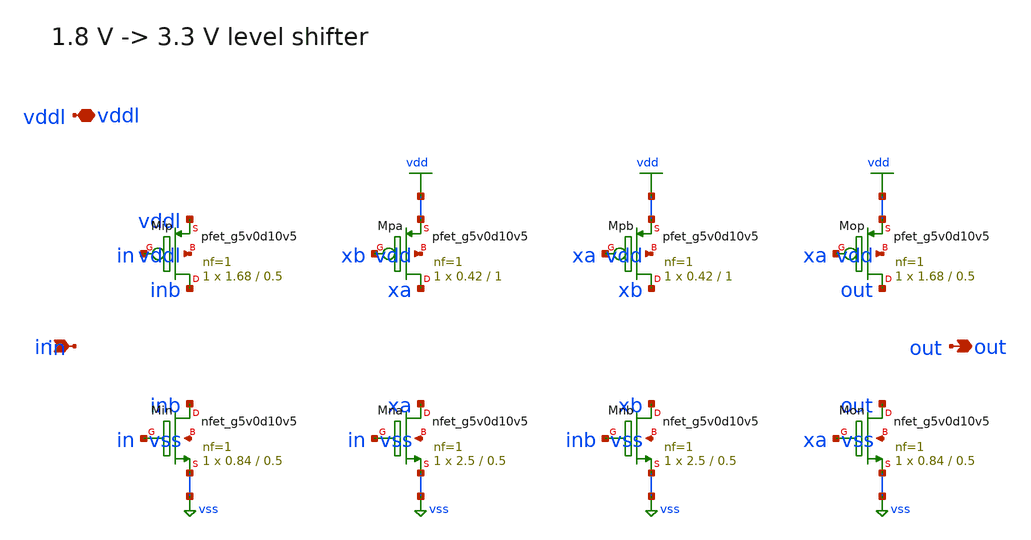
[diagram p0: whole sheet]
** sch_path: xschem/rt5w_lsup.sch
**.subckt rt5w_lsup in out vddl
*.ipin in
*.opin out
*.iopin vddl
XMip inb in vddl vddl sky130_fd_pr__pfet_g5v0d10v5 L=0.5 W=1.68 nf=1 ad=0.4872 as=0.4872 pd=3.94
+ ps=3.94 nrd=0.1726 nrs=0.1726 sa=0 sb=0 sd=0 mult=1 m=1
XMin inb in vss vss sky130_fd_pr__nfet_g5v0d10v5 L=0.5 W=0.84 nf=1 ad=0.2436 as=0.2436 pd=2.26
+ ps=2.26 nrd=0.3452 nrs=0.3452 sa=0 sb=0 sd=0 mult=1 m=1
XMpa xa xb vdd vdd sky130_fd_pr__pfet_g5v0d10v5 L=1 W=0.42 nf=1 ad=0.1218 as=0.1218 pd=1.42 ps=1.42
+ nrd=0.6905 nrs=0.6905 sa=0 sb=0 sd=0 mult=1 m=1
XMpb xb xa vdd vdd sky130_fd_pr__pfet_g5v0d10v5 L=1 W=0.42 nf=1 ad=0.1218 as=0.1218 pd=1.42 ps=1.42
+ nrd=0.6905 nrs=0.6905 sa=0 sb=0 sd=0 mult=1 m=1
XMna xa in vss vss sky130_fd_pr__nfet_g5v0d10v5 L=0.5 W=2.5 nf=1 ad=0.725 as=0.725 pd=5.58 ps=5.58
+ nrd=0.116 nrs=0.116 sa=0 sb=0 sd=0 mult=1 m=1
XMnb xb inb vss vss sky130_fd_pr__nfet_g5v0d10v5 L=0.5 W=2.5 nf=1 ad=0.725 as=0.725 pd=5.58 ps=5.58
+ nrd=0.116 nrs=0.116 sa=0 sb=0 sd=0 mult=1 m=1
XMop out xa vdd vdd sky130_fd_pr__pfet_g5v0d10v5 L=0.5 W=1.68 nf=1 ad=0.4872 as=0.4872 pd=3.94
+ ps=3.94 nrd=0.1726 nrs=0.1726 sa=0 sb=0 sd=0 mult=1 m=1
XMon out xa vss vss sky130_fd_pr__nfet_g5v0d10v5 L=0.5 W=0.84 nf=1 ad=0.2436 as=0.2436 pd=2.26
+ ps=2.26 nrd=0.3452 nrs=0.3452 sa=0 sb=0 sd=0 mult=1 m=1
**.ends
.GLOBAL vdd
.GLOBAL vss
.end
